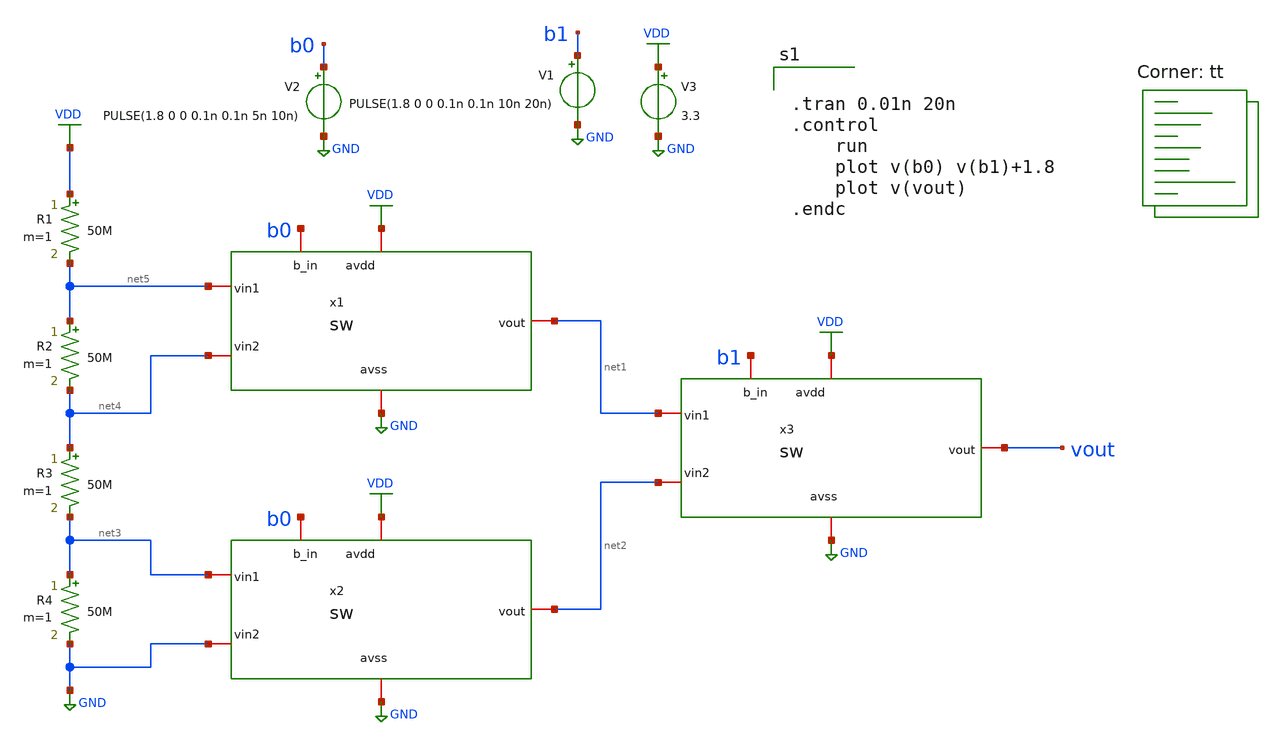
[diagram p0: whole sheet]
** sch_path: designs/libs/crossmem_ipn/dac4bits/sch/tb_DAC2BIT.sch
**.subckt tb_DAC2BIT
x1 VDD b0 GND net5 net1 net4 sw
x2 VDD b0 GND net3 net2 GND sw
x3 VDD b1 GND net1 vout net2 sw
V2 b0 GND PULSE(1.8 0 0 0.1n 0.1n 5n 10n)
V1 b1 GND PULSE(1.8 0 0 0.1n 0.1n 10n 20n)
V3 VDD GND 3.3
R1 VDD net5 50M m=1
R2 net5 net4 50M m=1
R3 net4 net3 50M m=1
R4 net3 GND 50M m=1
**** begin user architecture code
.lib $::SKYWATER_MODELS/sky130.lib.spice tt


.tran 0.01n 20n
.control
	run
	plot v(b0) v(b1)+1.8
	plot v(vout)
.endc



**** end user architecture code
**.ends

* expanding   symbol:  sw.sym # of pins=6
** sym_path: designs/libs/crossmem_ipn/dac4bits/sch/sw.sym
** sch_path: designs/libs/crossmem_ipn/dac4bits/sch/sw.sch
.subckt sw avdd b_in avss vin1 vout vin2
*.iopin avss
*.iopin vin1
*.iopin vout
*.iopin avdd
*.iopin vin2
*.iopin b_in
XM1 net1 b_in avss avss sky130_fd_pr__nfet_01v8 L=0.15 W=0.5 nf=1 ad='int((nf+1)/2) * W/nf * 0.29' as='int((nf+2)/2) * W/nf * 0.29'
+ pd='2*int((nf+1)/2) * (W/nf + 0.29)' ps='2*int((nf+2)/2) * (W/nf + 0.29)' nrd='0.29 / W' nrs='0.29 / W'
+ sa=0 sb=0 sd=0 mult=1 m=1
XM2 net1 b_in avdd avdd sky130_fd_pr__pfet_01v8 L=0.15 W=0.5 nf=1 ad='int((nf+1)/2) * W/nf * 0.29' as='int((nf+2)/2) * W/nf * 0.29'
+ pd='2*int((nf+1)/2) * (W/nf + 0.29)' ps='2*int((nf+2)/2) * (W/nf + 0.29)' nrd='0.29 / W' nrs='0.29 / W'
+ sa=0 sb=0 sd=0 mult=1 m=1
XM3 net2 net1 avss avss sky130_fd_pr__nfet_01v8 L=0.15 W=0.5 nf=1 ad='int((nf+1)/2) * W/nf * 0.29' as='int((nf+2)/2) * W/nf * 0.29'
+ pd='2*int((nf+1)/2) * (W/nf + 0.29)' ps='2*int((nf+2)/2) * (W/nf + 0.29)' nrd='0.29 / W' nrs='0.29 / W'
+ sa=0 sb=0 sd=0 mult=1 m=1
XM4 net2 net1 avdd avdd sky130_fd_pr__pfet_01v8 L=0.15 W=0.5 nf=1 ad='int((nf+1)/2) * W/nf * 0.29' as='int((nf+2)/2) * W/nf * 0.29'
+ pd='2*int((nf+1)/2) * (W/nf + 0.29)' ps='2*int((nf+2)/2) * (W/nf + 0.29)' nrd='0.29 / W' nrs='0.29 / W'
+ sa=0 sb=0 sd=0 mult=1 m=1
XM5 vout net1 vin1 avdd sky130_fd_pr__pfet_01v8 L=0.15 W=0.5 nf=1 ad='int((nf+1)/2) * W/nf * 0.29' as='int((nf+2)/2) * W/nf * 0.29'
+ pd='2*int((nf+1)/2) * (W/nf + 0.29)' ps='2*int((nf+2)/2) * (W/nf + 0.29)' nrd='0.29 / W' nrs='0.29 / W'
+ sa=0 sb=0 sd=0 mult=1 m=1
XM6 vout net1 vin2 avss sky130_fd_pr__nfet_01v8 L=0.15 W=0.5 nf=1 ad='int((nf+1)/2) * W/nf * 0.29' as='int((nf+2)/2) * W/nf * 0.29'
+ pd='2*int((nf+1)/2) * (W/nf + 0.29)' ps='2*int((nf+2)/2) * (W/nf + 0.29)' nrd='0.29 / W' nrs='0.29 / W'
+ sa=0 sb=0 sd=0 mult=1 m=1
XM7 vin1 net2 vout avss sky130_fd_pr__nfet_01v8 L=0.15 W=0.5 nf=1 ad='int((nf+1)/2) * W/nf * 0.29' as='int((nf+2)/2) * W/nf * 0.29'
+ pd='2*int((nf+1)/2) * (W/nf + 0.29)' ps='2*int((nf+2)/2) * (W/nf + 0.29)' nrd='0.29 / W' nrs='0.29 / W'
+ sa=0 sb=0 sd=0 mult=1 m=1
XM8 vin2 net2 vout avdd sky130_fd_pr__pfet_01v8 L=0.15 W=0.5 nf=1 ad='int((nf+1)/2) * W/nf * 0.29' as='int((nf+2)/2) * W/nf * 0.29'
+ pd='2*int((nf+1)/2) * (W/nf + 0.29)' ps='2*int((nf+2)/2) * (W/nf + 0.29)' nrd='0.29 / W' nrs='0.29 / W'
+ sa=0 sb=0 sd=0 mult=1 m=1
.ends

.GLOBAL GND
.GLOBAL VDD
.end
